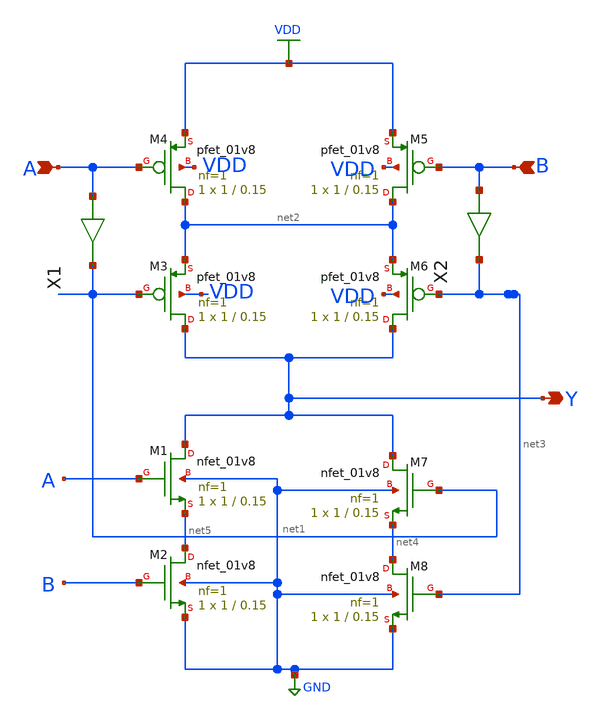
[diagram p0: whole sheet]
** sch_path: gates/XOR2.sch
**.subckt XOR2 A B Y
*.ipin A
*.ipin B
*.opin Y
XM1 Y A net5 GND sky130_fd_pr__nfet_01v8 L=0.15 W=1 nf=1 ad='int((nf+1)/2) * W/nf * 0.29' as='int((nf+2)/2) * W/nf * 0.29'
+ pd='2*int((nf+1)/2) * (W/nf + 0.29)' ps='2*int((nf+2)/2) * (W/nf + 0.29)' nrd='0.29 / W' nrs='0.29 / W'
+ sa=0 sb=0 sd=0 mult=1 m=1
XM2 net5 B GND GND sky130_fd_pr__nfet_01v8 L=0.15 W=1 nf=1 ad='int((nf+1)/2) * W/nf * 0.29' as='int((nf+2)/2) * W/nf * 0.29'
+ pd='2*int((nf+1)/2) * (W/nf + 0.29)' ps='2*int((nf+2)/2) * (W/nf + 0.29)' nrd='0.29 / W' nrs='0.29 / W'
+ sa=0 sb=0 sd=0 mult=1 m=1
XM3 Y net1 net2 VDD sky130_fd_pr__pfet_01v8 L=0.15 W=1 nf=1 ad='int((nf+1)/2) * W/nf * 0.29' as='int((nf+2)/2) * W/nf * 0.29'
+ pd='2*int((nf+1)/2) * (W/nf + 0.29)' ps='2*int((nf+2)/2) * (W/nf + 0.29)' nrd='0.29 / W' nrs='0.29 / W'
+ sa=0 sb=0 sd=0 mult=1 m=1
XM4 net2 A VDD VDD sky130_fd_pr__pfet_01v8 L=0.15 W=1 nf=1 ad='int((nf+1)/2) * W/nf * 0.29' as='int((nf+2)/2) * W/nf * 0.29'
+ pd='2*int((nf+1)/2) * (W/nf + 0.29)' ps='2*int((nf+2)/2) * (W/nf + 0.29)' nrd='0.29 / W' nrs='0.29 / W'
+ sa=0 sb=0 sd=0 mult=1 m=1
XM5 net2 B VDD VDD sky130_fd_pr__pfet_01v8 L=0.15 W=1 nf=1 ad='int((nf+1)/2) * W/nf * 0.29' as='int((nf+2)/2) * W/nf * 0.29'
+ pd='2*int((nf+1)/2) * (W/nf + 0.29)' ps='2*int((nf+2)/2) * (W/nf + 0.29)' nrd='0.29 / W' nrs='0.29 / W'
+ sa=0 sb=0 sd=0 mult=1 m=1
XM6 Y net3 net2 VDD sky130_fd_pr__pfet_01v8 L=0.15 W=1 nf=1 ad='int((nf+1)/2) * W/nf * 0.29' as='int((nf+2)/2) * W/nf * 0.29'
+ pd='2*int((nf+1)/2) * (W/nf + 0.29)' ps='2*int((nf+2)/2) * (W/nf + 0.29)' nrd='0.29 / W' nrs='0.29 / W'
+ sa=0 sb=0 sd=0 mult=1 m=1
XM7 Y net1 net4 GND sky130_fd_pr__nfet_01v8 L=0.15 W=1 nf=1 ad='int((nf+1)/2) * W/nf * 0.29' as='int((nf+2)/2) * W/nf * 0.29'
+ pd='2*int((nf+1)/2) * (W/nf + 0.29)' ps='2*int((nf+2)/2) * (W/nf + 0.29)' nrd='0.29 / W' nrs='0.29 / W'
+ sa=0 sb=0 sd=0 mult=1 m=1
XM8 net4 net3 GND GND sky130_fd_pr__nfet_01v8 L=0.15 W=1 nf=1 ad='int((nf+1)/2) * W/nf * 0.29' as='int((nf+2)/2) * W/nf * 0.29'
+ pd='2*int((nf+1)/2) * (W/nf + 0.29)' ps='2*int((nf+2)/2) * (W/nf + 0.29)' nrd='0.29 / W' nrs='0.29 / W'
+ sa=0 sb=0 sd=0 mult=1 m=1
X1 A net1 inv_vtc
X2 B net3 inv_vtc
**.ends

* expanding   symbol:  inv_vtc.sym # of pins=2
** sym_path: gates/inv_vtc.sym
** sch_path: gates/inv_vtc.sch
.subckt inv_vtc A Y
*.ipin A
*.opin Y
XM1 Y A VDD VDD sky130_fd_pr__pfet_01v8 L=0.15 W=2 nf=1 ad='int((nf+1)/2) * W/nf * 0.29' as='int((nf+2)/2) * W/nf * 0.29'
+ pd='2*int((nf+1)/2) * (W/nf + 0.29)' ps='2*int((nf+2)/2) * (W/nf + 0.29)' nrd='0.29 / W' nrs='0.29 / W'
+ sa=0 sb=0 sd=0 mult=1 m=1
XM2 Y A GND GND sky130_fd_pr__nfet_01v8 L=0.15 W=1 nf=1 ad='int((nf+1)/2) * W/nf * 0.29' as='int((nf+2)/2) * W/nf * 0.29'
+ pd='2*int((nf+1)/2) * (W/nf + 0.29)' ps='2*int((nf+2)/2) * (W/nf + 0.29)' nrd='0.29 / W' nrs='0.29 / W'
+ sa=0 sb=0 sd=0 mult=1 m=1
.ends

.GLOBAL VDD
.GLOBAL GND
.end
